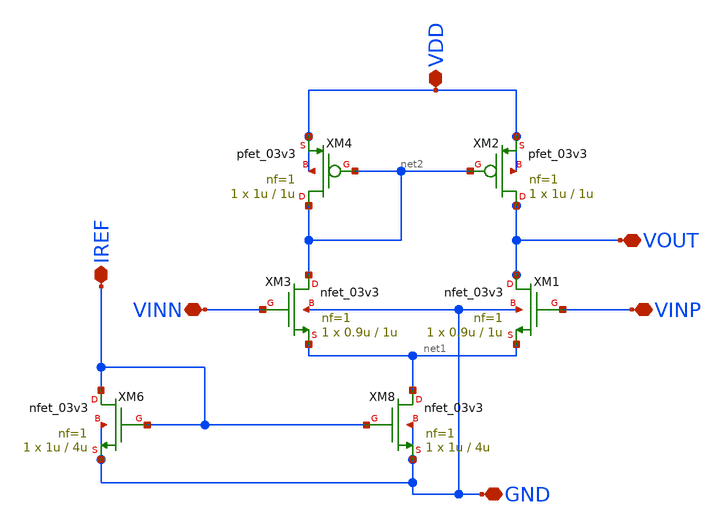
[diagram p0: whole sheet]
** sch_path: src/Pixel/OTA.sch
**.subckt OTA VINP VINN GND IREF VDD VOUT
*.iopin VINP
*.iopin VINN
*.iopin GND
*.iopin IREF
*.iopin VDD
*.iopin VOUT
XM2 VOUT net2 VDD VDD pfet_03v3 L=1u W=1u nf=1 ad='int((nf+1)/2) * W/nf * 0.18u' as='int((nf+2)/2) * W/nf * 0.18u'
+ pd='2*int((nf+1)/2) * (W/nf + 0.18u)' ps='2*int((nf+2)/2) * (W/nf + 0.18u)' nrd='0.18u / W' nrs='0.18u / W'
+ sa=0 sb=0 sd=0 m=1
XM4 net2 net2 VDD VDD pfet_03v3 L=1u W=1u nf=1 ad='int((nf+1)/2) * W/nf * 0.18u' as='int((nf+2)/2) * W/nf * 0.18u'
+ pd='2*int((nf+1)/2) * (W/nf + 0.18u)' ps='2*int((nf+2)/2) * (W/nf + 0.18u)' nrd='0.18u / W' nrs='0.18u / W'
+ sa=0 sb=0 sd=0 m=1
XM1 VOUT VINP net1 GND nfet_03v3 L=1u W=0.9u nf=1 ad='int((nf+1)/2) * W/nf * 0.18u' as='int((nf+2)/2) * W/nf * 0.18u'
+ pd='2*int((nf+1)/2) * (W/nf + 0.18u)' ps='2*int((nf+2)/2) * (W/nf + 0.18u)' nrd='0.18u / W' nrs='0.18u / W'
+ sa=0 sb=0 sd=0 m=1
XM3 net2 VINN net1 GND nfet_03v3 L=1u W=0.9u nf=1 ad='int((nf+1)/2) * W/nf * 0.18u' as='int((nf+2)/2) * W/nf * 0.18u'
+ pd='2*int((nf+1)/2) * (W/nf + 0.18u)' ps='2*int((nf+2)/2) * (W/nf + 0.18u)' nrd='0.18u / W' nrs='0.18u / W'
+ sa=0 sb=0 sd=0 m=1
XM8 net1 IREF GND GND nfet_03v3 L=4u W=1u nf=1 ad='int((nf+1)/2) * W/nf * 0.18u' as='int((nf+2)/2) * W/nf * 0.18u'
+ pd='2*int((nf+1)/2) * (W/nf + 0.18u)' ps='2*int((nf+2)/2) * (W/nf + 0.18u)' nrd='0.18u / W' nrs='0.18u / W'
+ sa=0 sb=0 sd=0 m=1
XM6 IREF IREF GND GND nfet_03v3 L=4u W=1u nf=1 ad='int((nf+1)/2) * W/nf * 0.18u' as='int((nf+2)/2) * W/nf * 0.18u'
+ pd='2*int((nf+1)/2) * (W/nf + 0.18u)' ps='2*int((nf+2)/2) * (W/nf + 0.18u)' nrd='0.18u / W' nrs='0.18u / W'
+ sa=0 sb=0 sd=0 m=1
**.ends
.end
